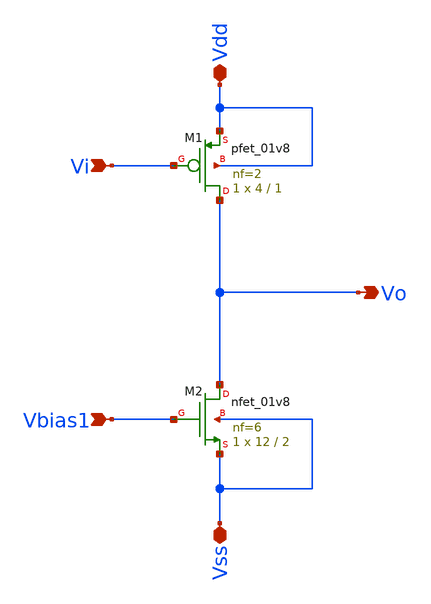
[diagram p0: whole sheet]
** sch_path: Circuits/Examples/MillerOpAmpCMMFB/CSAmp.sch
**.subckt CSAmp Vbias1 Vi Vdd Vss Vo
*.ipin Vbias1
*.ipin Vi
*.iopin Vdd
*.iopin Vss
*.opin Vo
XM1 Vo Vi Vdd Vdd sky130_fd_pr__pfet_01v8 L=1 W=4 nf=2 ad='int((nf+1)/2) * W/nf * 0.29' as='int((nf+2)/2) * W/nf * 0.29'
+ pd='2*int((nf+1)/2) * (W/nf + 0.29)' ps='2*int((nf+2)/2) * (W/nf + 0.29)' nrd='0.29 / W' nrs='0.29 / W'
+ sa=0 sb=0 sd=0 mult=1 m=1
XM2 Vo Vbias1 Vss Vss sky130_fd_pr__nfet_01v8 L=2 W=12 nf=6 ad='int((nf+1)/2) * W/nf * 0.29' as='int((nf+2)/2) * W/nf * 0.29'
+ pd='2*int((nf+1)/2) * (W/nf + 0.29)' ps='2*int((nf+2)/2) * (W/nf + 0.29)' nrd='0.29 / W' nrs='0.29 / W'
+ sa=0 sb=0 sd=0 mult=1 m=1
**.ends
.end
